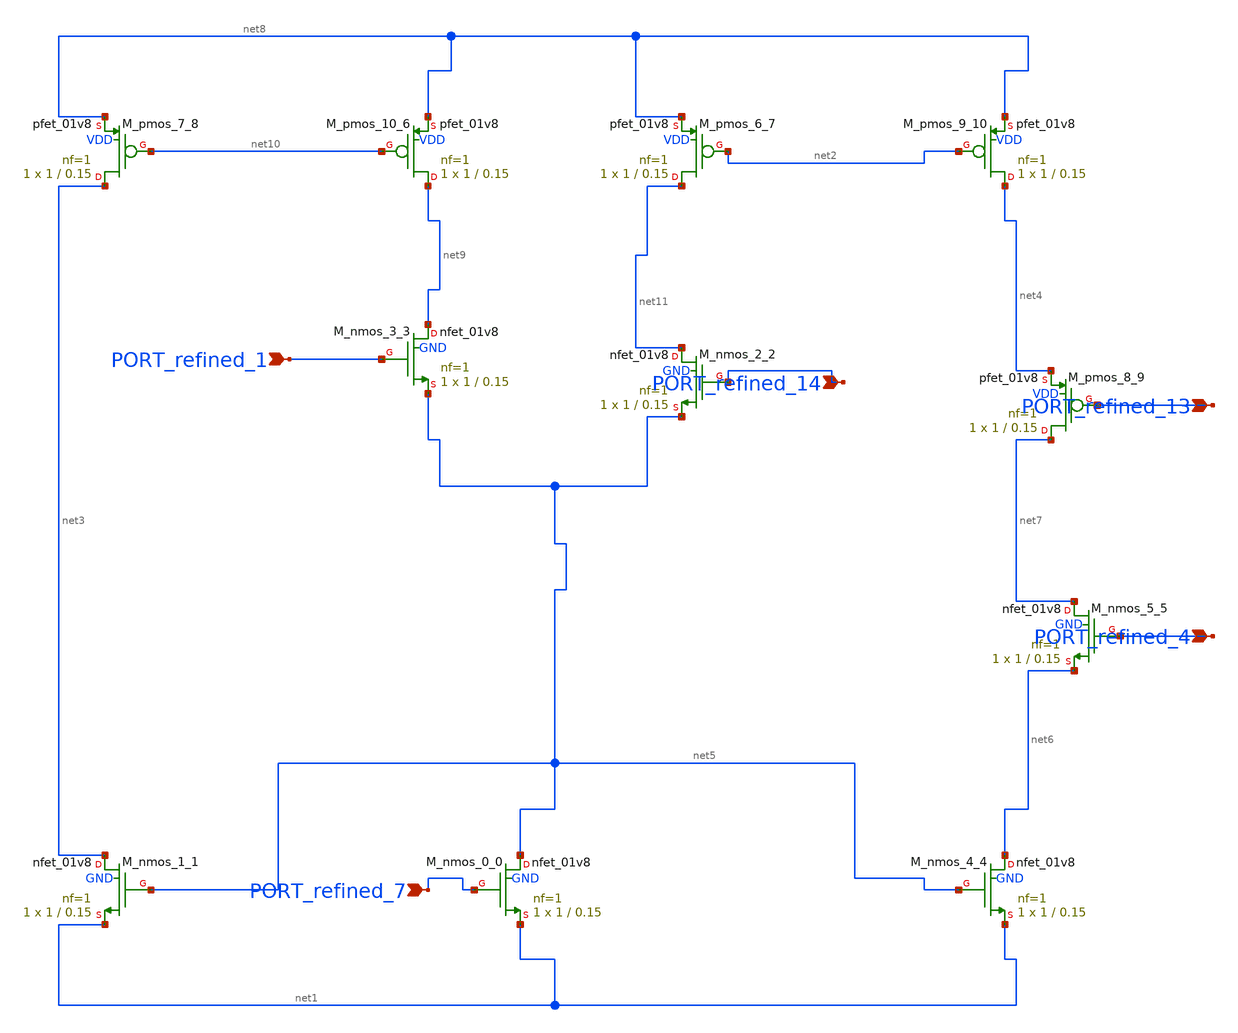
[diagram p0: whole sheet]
** sch_path: schematics/SchemGen/10_11591_ijece_v12i2_pp2158-2168_04_001.sch
**.subckt 10_11591_ijece_v12i2_pp2158-2168_04_001 PORT_refined_14 PORT_refined_1 PORT_refined_13
*+ PORT_refined_7 PORT_refined_4
*.ipin PORT_refined_14
*.ipin PORT_refined_1
*.ipin PORT_refined_13
*.ipin PORT_refined_7
*.ipin PORT_refined_4
XM_nmos_0_0 net5 PORT_refined_7 net1 GND sky130_fd_pr__nfet_01v8 L=0.15 W=1 nf=1 ad='int((1 + 1)/2) * 1 / 1 * 0.29'
+ as='int((1 + 2)/2) * 1 / 1 * 0.29' pd='2*int((1 + 1)/2) * (1 / 1 + 0.29)' ps='2*int((1 + 2)/2) * (1 / 1 + 0.29)'
+ nrd='0.29 / 1 ' nrs='0.29 / 1 ' sa=0 sb=0 sd=0 mult=1 m=1
XM_nmos_1_1 net3 net5 net1 GND sky130_fd_pr__nfet_01v8 L=0.15 W=1 nf=1 ad='int((1 + 1)/2) * 1 / 1 * 0.29'
+ as='int((1 + 2)/2) * 1 / 1 * 0.29' pd='2*int((1 + 1)/2) * (1 / 1 + 0.29)' ps='2*int((1 + 2)/2) * (1 / 1 + 0.29)'
+ nrd='0.29 / 1 ' nrs='0.29 / 1 ' sa=0 sb=0 sd=0 mult=1 m=1
XM_nmos_2_2 net11 PORT_refined_14 net5 GND sky130_fd_pr__nfet_01v8 L=0.15 W=1 nf=1 ad='int((1 + 1)/2) * 1 / 1 * 0.29'
+ as='int((1 + 2)/2) * 1 / 1 * 0.29' pd='2*int((1 + 1)/2) * (1 / 1 + 0.29)' ps='2*int((1 + 2)/2) * (1 / 1 + 0.29)'
+ nrd='0.29 / 1 ' nrs='0.29 / 1 ' sa=0 sb=0 sd=0 mult=1 m=1
XM_nmos_3_3 net9 PORT_refined_1 net5 GND sky130_fd_pr__nfet_01v8 L=0.15 W=1 nf=1 ad='int((1 + 1)/2) * 1 / 1 * 0.29'
+ as='int((1 + 2)/2) * 1 / 1 * 0.29' pd='2*int((1 + 1)/2) * (1 / 1 + 0.29)' ps='2*int((1 + 2)/2) * (1 / 1 + 0.29)'
+ nrd='0.29 / 1 ' nrs='0.29 / 1 ' sa=0 sb=0 sd=0 mult=1 m=1
XM_nmos_4_4 net6 net5 net1 GND sky130_fd_pr__nfet_01v8 L=0.15 W=1 nf=1 ad='int((1 + 1)/2) * 1 / 1 * 0.29'
+ as='int((1 + 2)/2) * 1 / 1 * 0.29' pd='2*int((1 + 1)/2) * (1 / 1 + 0.29)' ps='2*int((1 + 2)/2) * (1 / 1 + 0.29)'
+ nrd='0.29 / 1 ' nrs='0.29 / 1 ' sa=0 sb=0 sd=0 mult=1 m=1
XM_nmos_5_5 net7 PORT_refined_4 net6 GND sky130_fd_pr__nfet_01v8 L=0.15 W=1 nf=1 ad='int((1 + 1)/2) * 1 / 1 * 0.29'
+ as='int((1 + 2)/2) * 1 / 1 * 0.29' pd='2*int((1 + 1)/2) * (1 / 1 + 0.29)' ps='2*int((1 + 2)/2) * (1 / 1 + 0.29)'
+ nrd='0.29 / 1 ' nrs='0.29 / 1 ' sa=0 sb=0 sd=0 mult=1 m=1
XM_pmos_10_6 net9 net10 net8 VDD sky130_fd_pr__pfet_01v8 L=0.15 W=1 nf=1 ad='int((1 + 1)/2) * 1 / 1 * 0.29'
+ as='int((1 + 2)/2) * 1 / 1 * 0.29' pd='2*int((1 + 1)/2) * (1 / 1 + 0.29)' ps='2*int((1 + 2)/2) * (1 / 1 + 0.29)'
+ nrd='0.29 / 1 ' nrs='0.29 / 1 ' sa=0 sb=0 sd=0 mult=1 m=1
XM_pmos_6_7 net11 net2 net8 VDD sky130_fd_pr__pfet_01v8 L=0.15 W=1 nf=1 ad='int((1 + 1)/2) * 1 / 1 * 0.29'
+ as='int((1 + 2)/2) * 1 / 1 * 0.29' pd='2*int((1 + 1)/2) * (1 / 1 + 0.29)' ps='2*int((1 + 2)/2) * (1 / 1 + 0.29)'
+ nrd='0.29 / 1 ' nrs='0.29 / 1 ' sa=0 sb=0 sd=0 mult=1 m=1
XM_pmos_7_8 net3 net10 net8 VDD sky130_fd_pr__pfet_01v8 L=0.15 W=1 nf=1 ad='int((1 + 1)/2) * 1 / 1 * 0.29'
+ as='int((1 + 2)/2) * 1 / 1 * 0.29' pd='2*int((1 + 1)/2) * (1 / 1 + 0.29)' ps='2*int((1 + 2)/2) * (1 / 1 + 0.29)'
+ nrd='0.29 / 1 ' nrs='0.29 / 1 ' sa=0 sb=0 sd=0 mult=1 m=1
XM_pmos_8_9 net7 PORT_refined_13 net4 VDD sky130_fd_pr__pfet_01v8 L=0.15 W=1 nf=1 ad='int((1 + 1)/2) * 1 / 1 * 0.29'
+ as='int((1 + 2)/2) * 1 / 1 * 0.29' pd='2*int((1 + 1)/2) * (1 / 1 + 0.29)' ps='2*int((1 + 2)/2) * (1 / 1 + 0.29)'
+ nrd='0.29 / 1 ' nrs='0.29 / 1 ' sa=0 sb=0 sd=0 mult=1 m=1
XM_pmos_9_10 net4 net2 net8 VDD sky130_fd_pr__pfet_01v8 L=0.15 W=1 nf=1 ad='int((1 + 1)/2) * 1 / 1 * 0.29'
+ as='int((1 + 2)/2) * 1 / 1 * 0.29' pd='2*int((1 + 1)/2) * (1 / 1 + 0.29)' ps='2*int((1 + 2)/2) * (1 / 1 + 0.29)'
+ nrd='0.29 / 1 ' nrs='0.29 / 1 ' sa=0 sb=0 sd=0 mult=1 m=1
**.ends
.end
